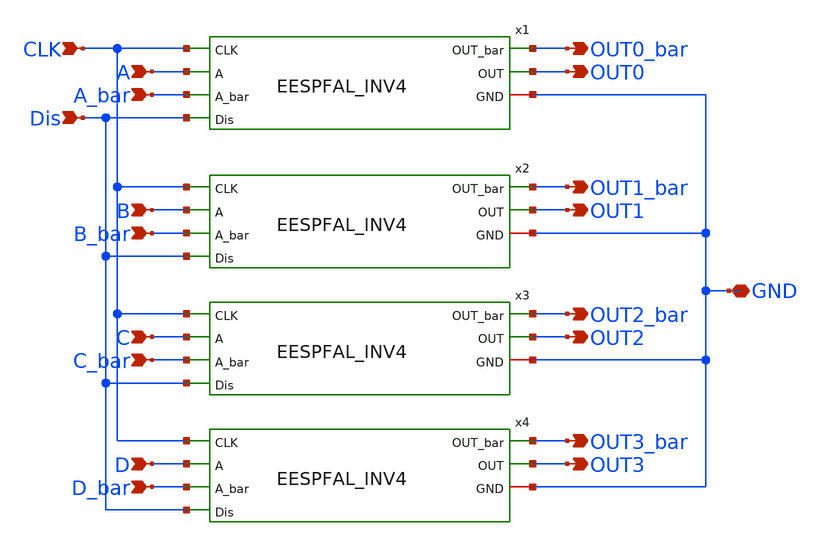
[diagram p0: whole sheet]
** sch_path: skywater_stuff/EESPFAL_4in_Buffer.sch
**.subckt EESPFAL_4in_Buffer A A_bar B B_bar C C_bar D D_bar OUT0 OUT0_bar OUT1 OUT1_bar OUT2
*+ OUT2_bar OUT3 OUT3_bar Dis GND CLK
*.ipin A
*.ipin A_bar
*.ipin B
*.ipin B_bar
*.ipin C
*.ipin C_bar
*.ipin D
*.ipin D_bar
*.opin OUT0
*.opin OUT0_bar
*.opin OUT1
*.opin OUT1_bar
*.opin OUT2
*.opin OUT2_bar
*.opin OUT3
*.opin OUT3_bar
*.ipin Dis
*.iopin GND
*.ipin CLK
x1 A A_bar OUT0 OUT0_bar Dis GND CLK EESPFAL_INV4
x2 B B_bar OUT1 OUT1_bar Dis GND CLK EESPFAL_INV4
x3 C C_bar OUT2 OUT2_bar Dis GND CLK EESPFAL_INV4
x4 D D_bar OUT3 OUT3_bar Dis GND CLK EESPFAL_INV4
**.ends
.end
